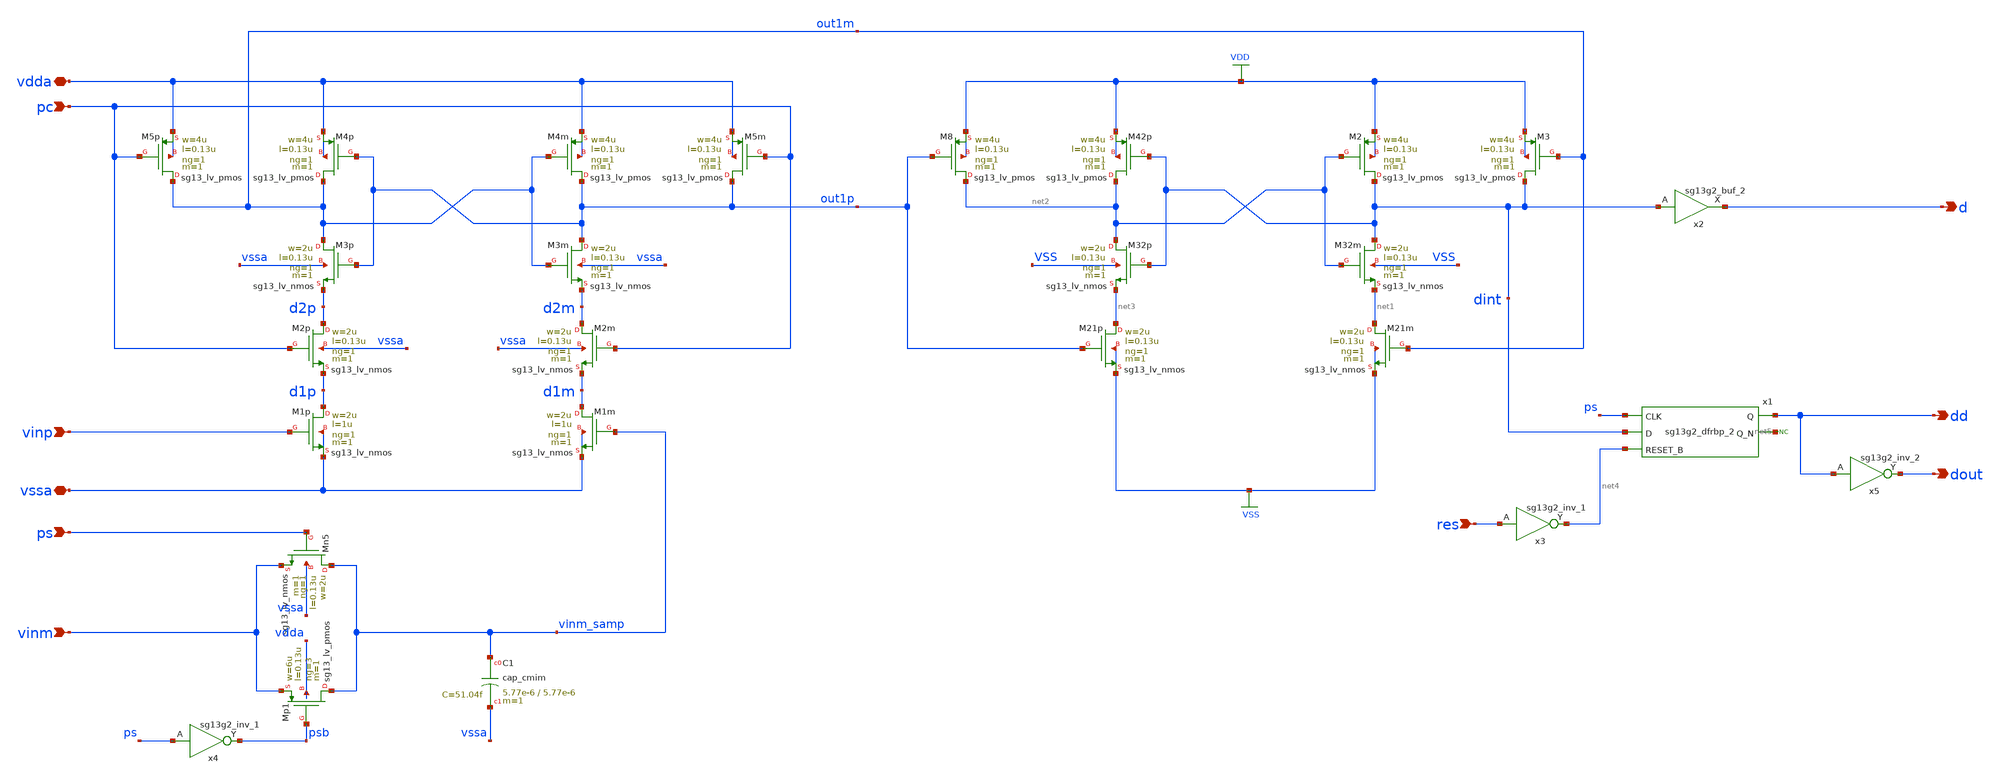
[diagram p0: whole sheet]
** sch_path: 5_Design/3_Real_circuits/template_comp.sch
* IHP-GmbH/IHP-Open-PDK/ihp-sg13g2/libs.tech/xschem/sg13g2_stdcells/sg13g2_inv_2.sch:
* Copyright 2023 IHP PDK Authors
* Licensed under the Apache License, Version 2.0 (the "License");
**.subckt template_comp d pc vssa vdda ps res dd vinm vinp dout
*.opin d
*.ipin pc
*.iopin vssa
*.iopin vdda
*.ipin ps
*.ipin res
*.opin dd
*.ipin vinm
*.ipin vinp
*.opin dout
XM3m out1p out1m d2m vssa sg13_lv_nmos w=2u l=0.13u ng=1 m=1 mm_ok=1
XM4m out1p out1m vdda vdda sg13_lv_pmos w=4u l=0.13u ng=1 m=1 mm_ok=1
XM5m out1p pc vdda vdda sg13_lv_pmos w=4u l=0.13u ng=1 m=1 mm_ok=1
XM2m d2m pc d1m vssa sg13_lv_nmos w=2u l=0.13u ng=1 m=1 mm_ok=1
XM1m d1m vinm_samp vssa vssa sg13_lv_nmos w=2u l=1u ng=1 m=1 mm_ok=1
XM3p out1m out1p d2p vssa sg13_lv_nmos w=2u l=0.13u ng=1 m=1 mm_ok=1
XM4p out1m out1p vdda vdda sg13_lv_pmos w=4u l=0.13u ng=1 m=1 mm_ok=1
XM5p out1m pc vdda vdda sg13_lv_pmos w=4u l=0.13u ng=1 m=1 mm_ok=1
XM2p d2p pc d1p vssa sg13_lv_nmos w=2u l=0.13u ng=1 m=1 mm_ok=1
XM1p d1p vinp vssa vssa sg13_lv_nmos w=2u l=1u ng=1 m=1 mm_ok=1
XM32m dint net2 net1 VSS sg13_lv_nmos w=2u l=0.13u ng=1 m=1 mm_ok=1
XM2 dint net2 VDD VDD sg13_lv_pmos w=4u l=0.13u ng=1 m=1 mm_ok=1
XM3 dint out1m VDD VDD sg13_lv_pmos w=4u l=0.13u ng=1 m=1 mm_ok=1
XM21m net1 out1m VSS VSS sg13_lv_nmos w=2u l=0.13u ng=1 m=1 mm_ok=1
XM32p net2 dint net3 VSS sg13_lv_nmos w=2u l=0.13u ng=1 m=1 mm_ok=1
XM42p net2 dint VDD VDD sg13_lv_pmos w=4u l=0.13u ng=1 m=1 mm_ok=1
XM8 net2 out1p VDD VDD sg13_lv_pmos w=4u l=0.13u ng=1 m=1 mm_ok=1
XM21p net3 out1p VSS VSS sg13_lv_nmos w=2u l=0.13u ng=1 m=1 mm_ok=1
x1 dd net5 ps dint net4 VDD VSS sg13g2_dfrbp_2
x2 d dint VDD VSS sg13g2_buf_2
x3 net4 res VDD VSS sg13g2_inv_1
XMp1 vinm_samp psb vinm vdda sg13_lv_pmos w=6u l=0.13u ng=3 m=1 mm_ok=1
XMn5 vinm_samp ps vinm vssa sg13_lv_nmos w=2u l=0.13u ng=1 m=1 mm_ok=1
XC1 vinm_samp vssa cap_cmim w=5.77e-6 l=5.77e-6 m=1 mm_ok=1
x4 psb ps VDD VSS sg13g2_inv_1
x5 dout dd VDD VSS sg13g2_inv_2
* noconn #net5
**.ends

* expanding   symbol:  sg13g2_stdcells/sg13g2_dfrbp_2.sym # of pins=5
** sym_path: sg13g2_stdcells/sg13g2_dfrbp_2.sym
** sch_path: sg13g2_stdcells/sg13g2_dfrbp_2.sch
.subckt sg13g2_dfrbp_2 Q Q_N CLK D RESET_B VDD VSS
*.ipin D
*.ipin RESET_B
*.ipin CLK
*.opin Q
*.opin Q_N
*.iopin VDD
*.iopin VSS
XM1 Db D net12 VSS sg13_lv_nmos w=420.00n l=130.00n ng=1 m=1 mm_ok=1
XM2 net12 RESET_B VSS VSS sg13_lv_nmos w=420.00n l=130.00n ng=1 m=1 mm_ok=1
XM3 net2 clkneg net11 VSS sg13_lv_nmos w=420.00n l=130.00n ng=1 m=1 mm_ok=1
XM4 net11 net3 VSS VSS sg13_lv_nmos w=420.00n l=130.00n ng=1 m=1 mm_ok=1
XM5 net3 net2 net7 VSS sg13_lv_nmos w=420.00n l=130.00n ng=1 m=1 mm_ok=1
XM6 net7 RESET_B VSS VSS sg13_lv_nmos w=420.00n l=130.00n ng=1 m=1 mm_ok=1
XM7 Q_N net2 VSS VSS sg13_lv_nmos w=1.48u l=130.00n ng=2 m=1 mm_ok=1
XM8 net1 net2 VSS VSS sg13_lv_nmos w=640.00n l=130.00n ng=1 m=1 mm_ok=1
XM9 Q net1 VSS VSS sg13_lv_nmos w=1.48u l=130.00n ng=2 m=1 mm_ok=1
XM10 clkneg CLK VSS VSS sg13_lv_nmos w=740.00n l=130.00n ng=1 m=1 mm_ok=1
XM11 clkpos clkneg VSS VSS sg13_lv_nmos w=740.00n l=130.00n ng=1 m=1 mm_ok=1
XM12 Db clkneg net4 VSS sg13_lv_nmos w=420.00n l=130.00n ng=1 m=1 mm_ok=1
XM13 net4 clkpos net10 VSS sg13_lv_nmos w=420.00n l=130.00n ng=1 m=1 mm_ok=1
XM14 net10 net5 net6 VSS sg13_lv_nmos w=420.00n l=130.00n ng=1 m=1 mm_ok=1
XM15 net6 RESET_B VSS VSS sg13_lv_nmos w=420.00n l=130.00n ng=1 m=1 mm_ok=1
XM16 net5 net4 VSS VSS sg13_lv_nmos w=740.00n l=130.00n ng=1 m=1 mm_ok=1
XM17 net5 clkpos net2 VSS sg13_lv_nmos w=740.00n l=130.00n ng=1 m=1 mm_ok=1
XM18 Db RESET_B VDD VDD sg13_lv_pmos w=420.00n l=130.00n ng=1 m=1 mm_ok=1
XM19 Db D VDD VDD sg13_lv_pmos w=420.00n l=130.00n ng=1 m=1 mm_ok=1
XM20 net9 net3 VDD VDD sg13_lv_pmos w=420.00n l=130.00n ng=1 m=1 mm_ok=1
XM21 net2 clkpos net9 VDD sg13_lv_pmos w=420.00n l=130.00n ng=1 m=1 mm_ok=1
XM22 net3 net2 VDD VDD sg13_lv_pmos w=420.00n l=130.00n ng=1 m=1 mm_ok=1
XM23 net3 RESET_B VDD VDD sg13_lv_pmos w=420.00n l=130.00n ng=1 m=1 mm_ok=1
XM24 Q_N net2 VDD VDD sg13_lv_pmos w=2.24u l=130.00n ng=2 m=1 mm_ok=1
XM25 net1 net2 VDD VDD sg13_lv_pmos w=1.000u l=130.00n ng=1 m=1 mm_ok=1
XM26 Q net1 VDD VDD sg13_lv_pmos w=2.24u l=130.00n ng=2 m=1 mm_ok=1
XM27 clkneg CLK VDD VDD sg13_lv_pmos w=1.12u l=130.00n ng=1 m=1 mm_ok=1
XM28 clkpos clkneg VDD VDD sg13_lv_pmos w=1.12u l=130.00n ng=1 m=1 mm_ok=1
XM29 Db clkpos net4 VDD sg13_lv_pmos w=420.00n l=130.00n ng=1 m=1 mm_ok=1
XM30 net8 net5 VDD VDD sg13_lv_pmos w=420.00n l=130.00n ng=1 m=1 mm_ok=1
XM31 net4 clkneg net8 VDD sg13_lv_pmos w=420.00n l=130.00n ng=1 m=1 mm_ok=1
XM32 net4 RESET_B VDD VDD sg13_lv_pmos w=420.00n l=130.00n ng=1 m=1 mm_ok=1
XM33 net5 net4 VDD VDD sg13_lv_pmos w=1.000u l=130.00n ng=1 m=1 mm_ok=1
XM34 net5 clkneg net2 VDD sg13_lv_pmos w=1.000u l=130.00n ng=1 m=1 mm_ok=1
.ends


* expanding   symbol:  sg13g2_stdcells/sg13g2_buf_2.sym # of pins=2
** sym_path: sg13g2_stdcells/sg13g2_buf_2.sym
** sch_path: sg13g2_stdcells/sg13g2_buf_2.sch
.subckt sg13g2_buf_2 X A VDD VSS
*.ipin A
*.opin X
*.iopin VDD
*.iopin VSS
XM1 net1 A VSS VSS sg13_lv_nmos w=640.00n l=130.00n ng=1 m=1 mm_ok=1
XM2 X net1 VSS VSS sg13_lv_nmos w=1.48u l=130.00n ng=2 m=1 mm_ok=1
XM3 net1 A VDD VDD sg13_lv_pmos w=1.000u l=130.00n ng=1 m=1 mm_ok=1
XM4 X net1 VDD VDD sg13_lv_pmos w=2.24u l=130.00n ng=2 m=1 mm_ok=1
.ends


* expanding   symbol:  sg13g2_stdcells/sg13g2_inv_1.sym # of pins=2
** sym_path: sg13g2_stdcells/sg13g2_inv_1.sym
** sch_path: sg13g2_stdcells/sg13g2_inv_1.sch
.subckt sg13g2_inv_1 Y A VDD VSS
*.opin Y
*.ipin A
*.iopin VDD
*.iopin VSS
XM1 Y A VSS VSS sg13_lv_nmos w=740.00n l=130.00n ng=1 m=1 mm_ok=1
XM2 Y A VDD VDD sg13_lv_pmos w=1.12u l=130.00n ng=1 m=1 mm_ok=1
.ends


* expanding   symbol:  sg13g2_stdcells/sg13g2_inv_2.sym # of pins=2
** sym_path: sg13g2_stdcells/sg13g2_inv_2.sym
** sch_path: sg13g2_stdcells/sg13g2_inv_2.sch
.subckt sg13g2_inv_2 Y A VDD VSS
*.opin Y
*.ipin A
*.iopin VDD
*.iopin VSS
XM1 Y A VSS VSS sg13_lv_nmos w=1.48u l=130.00n ng=2 m=1 mm_ok=1
XM2 Y A VDD VDD sg13_lv_pmos w=2.24u l=130.00n ng=2 m=1 mm_ok=1
.ends

.GLOBAL VDD
.GLOBAL VSS
.end
